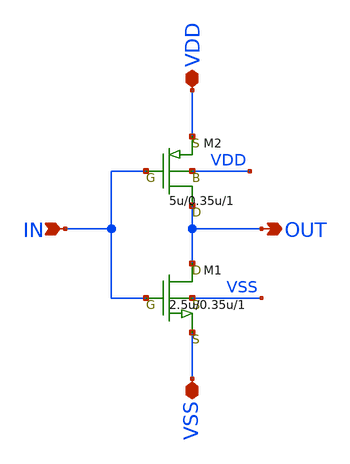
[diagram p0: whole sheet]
** sch_path: INV.sch
**.subckt INV OUT IN VDD VSS
*.opin OUT
*.ipin IN
*.iopin VDD
*.iopin VSS
M2 OUT IN VDD VDD pch w=5u l=0.35u as=0 ps=0 ad=0 pd=0 m=1
M1 OUT IN VSS VSS nch w=2.5u l=0.35u as=0 ps=0 ad=0 pd=0 m=1
**.ends
.end
